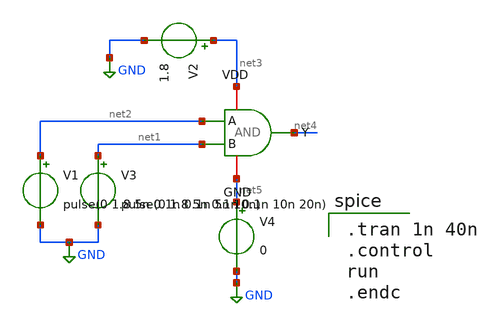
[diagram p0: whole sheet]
** sch_path: FinalProj/AND_testCKT.sch
**.subckt AND_testCKT
V1 net2 GND pulse(0 1.8 5n 0.1n 0.1n 5n 10n)
V3 net1 GND pulse(0 1.8 5n 0.1n 0.1n 10n 20n)
V2 net3 GND 1.8
V4 net5 GND 0
x1 net3 net2 net4 net1 net5 AND
**** begin user architecture code
 .lib $::SKYWATER_MODELS/sky130.lib.spice tt

.tran 1n 40n
.control
run
.endc

**** end user architecture code
**.ends

* expanding   symbol:  workspace/FinalProj/AND.sym # of pins=5
** sym_path: FinalProj/AND.sym
** sch_path: FinalProj/AND.sch
.subckt AND VDD A Y B GND
*.ipin A
*.ipin B
*.iopin VDD
*.iopin GND
*.opin Y
x1 VDD net1 B A GND NAND
x2 VDD net1 Y GND Inv
.ends


* expanding   symbol:  workspace/FinalProj/NAND.sym # of pins=5
** sym_path: FinalProj/NAND.sym
** sch_path: FinalProj/NAND.sch
.subckt NAND VDD Y B A GND
*.ipin A
*.ipin B
*.iopin VDD
*.iopin GND
*.opin Y
XM1 Y B VDD VDD sky130_fd_pr__pfet_01v8 L=0.5 W=2 nf=1 ad='int((nf+1)/2) * W/nf * 0.29' as='int((nf+2)/2) * W/nf * 0.29'
+ pd='2*int((nf+1)/2) * (W/nf + 0.29)' ps='2*int((nf+2)/2) * (W/nf + 0.29)' nrd='0.29 / W' nrs='0.29 / W'
+ sa=0 sb=0 sd=0 mult=1 m=1
XM2 Y A VDD VDD sky130_fd_pr__pfet_01v8 L=0.5 W=2 nf=1 ad='int((nf+1)/2) * W/nf * 0.29' as='int((nf+2)/2) * W/nf * 0.29'
+ pd='2*int((nf+1)/2) * (W/nf + 0.29)' ps='2*int((nf+2)/2) * (W/nf + 0.29)' nrd='0.29 / W' nrs='0.29 / W'
+ sa=0 sb=0 sd=0 mult=1 m=1
XM3 Y B net1 GND sky130_fd_pr__nfet_01v8 L=0.5 W=2 nf=1 ad='int((nf+1)/2) * W/nf * 0.29' as='int((nf+2)/2) * W/nf * 0.29'
+ pd='2*int((nf+1)/2) * (W/nf + 0.29)' ps='2*int((nf+2)/2) * (W/nf + 0.29)' nrd='0.29 / W' nrs='0.29 / W'
+ sa=0 sb=0 sd=0 mult=1 m=1
XM4 net1 A GND GND sky130_fd_pr__nfet_01v8 L=0.5 W=2 nf=1 ad='int((nf+1)/2) * W/nf * 0.29' as='int((nf+2)/2) * W/nf * 0.29'
+ pd='2*int((nf+1)/2) * (W/nf + 0.29)' ps='2*int((nf+2)/2) * (W/nf + 0.29)' nrd='0.29 / W' nrs='0.29 / W'
+ sa=0 sb=0 sd=0 mult=1 m=1
.ends


* expanding   symbol:  workspace/FinalProj/Inv.sym # of pins=4
** sym_path: FinalProj/Inv.sym
** sch_path: FinalProj/Inv.sch
.subckt Inv VDD A Y GND
*.ipin A
*.iopin GND
*.iopin VDD
*.opin Y
XM1 Y A VDD VDD sky130_fd_pr__pfet_01v8 L=0.5 W=1 nf=1 ad='int((nf+1)/2) * W/nf * 0.29' as='int((nf+2)/2) * W/nf * 0.29'
+ pd='2*int((nf+1)/2) * (W/nf + 0.29)' ps='2*int((nf+2)/2) * (W/nf + 0.29)' nrd='0.29 / W' nrs='0.29 / W'
+ sa=0 sb=0 sd=0 mult=1 m=1
XM2 Y A GND GND sky130_fd_pr__nfet_01v8 L=0.5 W=0.5 nf=1 ad='int((nf+1)/2) * W/nf * 0.29' as='int((nf+2)/2) * W/nf * 0.29'
+ pd='2*int((nf+1)/2) * (W/nf + 0.29)' ps='2*int((nf+2)/2) * (W/nf + 0.29)' nrd='0.29 / W' nrs='0.29 / W'
+ sa=0 sb=0 sd=0 mult=1 m=1
.ends

.GLOBAL GND
.end
